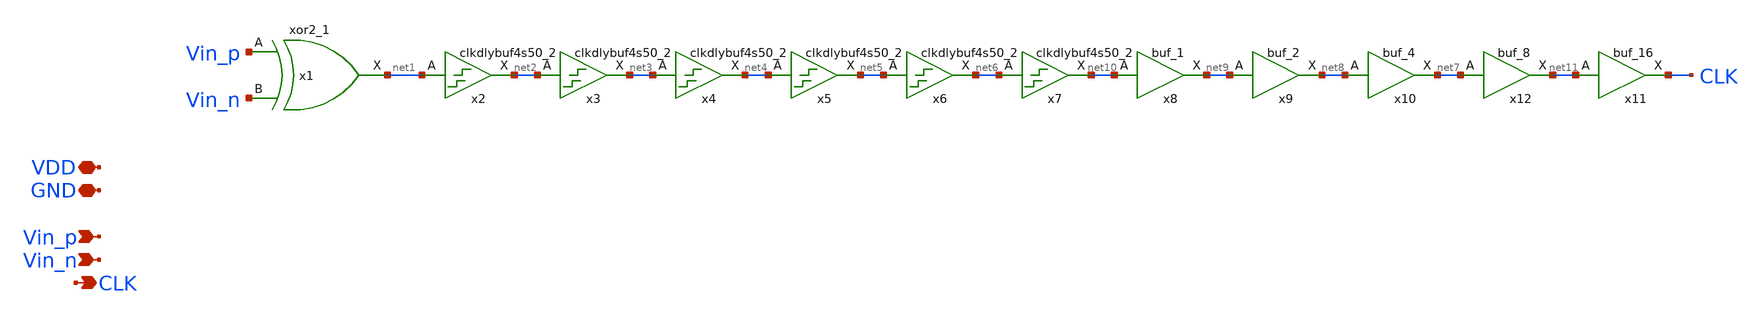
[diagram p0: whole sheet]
** sch_path: xschem/xor_clk_gen.sch
**.subckt xor_clk_gen VDD GND Vin_p CLK Vin_n
*.iopin VDD
*.iopin GND
*.ipin Vin_p
*.opin CLK
*.ipin Vin_n
x1 Vin_p Vin_n GND GND VDD VDD net1 sky130_fd_sc_hd__xor2_1
x2 net1 GND GND VDD VDD net2 sky130_fd_sc_hd__clkdlybuf4s50_2
x3 net2 GND GND VDD VDD net3 sky130_fd_sc_hd__clkdlybuf4s50_2
x4 net3 GND GND VDD VDD net4 sky130_fd_sc_hd__clkdlybuf4s50_2
x5 net4 GND GND VDD VDD net5 sky130_fd_sc_hd__clkdlybuf4s50_2
x6 net5 GND GND VDD VDD net6 sky130_fd_sc_hd__clkdlybuf4s50_2
x7 net6 GND GND VDD VDD net10 sky130_fd_sc_hd__clkdlybuf4s50_2
x8 net10 GND GND VDD VDD net9 sky130_fd_sc_hd__buf_1
x9 net9 GND GND VDD VDD net8 sky130_fd_sc_hd__buf_2
x10 net8 GND GND VDD VDD net7 sky130_fd_sc_hd__buf_4
x12 net7 GND GND VDD VDD net11 sky130_fd_sc_hd__buf_8
x11 net11 GND GND VDD VDD CLK sky130_fd_sc_hd__buf_16
**.ends
.end
